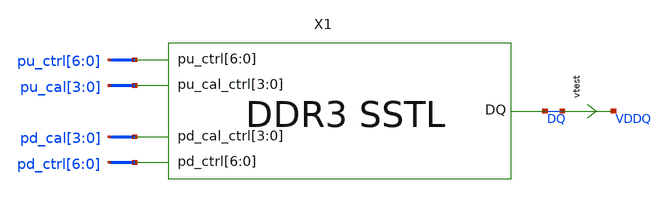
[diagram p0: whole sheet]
** sch_path: schem/sstl_res_tb.sch
* Copyright 2021 Stefan Frederik Schippers
* Licensed under the Apache License, Version 2.0 (the "License");
* you may not use this file except in compliance with the License.
* You may obtain a copy of the License at
* https://www.apache.org/licenses/LICENSE-2.0
* Unless required by applicable law or agreed to in writing, software
* distributed under the License is distributed on an "AS IS" BASIS,
* WITHOUT WARRANTIES OR CONDITIONS OF ANY KIND, either express or implied.
* See the License for the specific language governing permissions and
* limitations under the License.
**.subckt sstl_res_tb
vtest DQ VDDQ 0
.save i(vtest)
X1 DQ pd_ctrl[6] pd_ctrl[5] pd_ctrl[4] pd_ctrl[3] pd_ctrl[2] pd_ctrl[1] pd_ctrl[0] pu_ctrl[6]
+ pu_ctrl[5] pu_ctrl[4] pu_ctrl[3] pu_ctrl[2] pu_ctrl[1] pu_ctrl[0] pd_cal[3] pd_cal[2] pd_cal[1] pd_cal[0]
+ pu_cal[3] pu_cal[2] pu_cal[1] pu_cal[0] SSTL
**** begin user architecture code
 ** Local library links to pdk
.lib ./sky130/libs/SED_process_SED_lib.spice SED_process_SED
.include $::SKYWATER_STDCELLS/sky130_fd_sc_hd.spice

**** end user architecture code
**.ends

* expanding   symbol:  schem/SSTL.sym # of pins=5
** sym_path: schem/SSTL.sym
** sch_path: schem/SSTL.sch
.subckt SSTL DQ pd_ctrl[6] pd_ctrl[5] pd_ctrl[4] pd_ctrl[3] pd_ctrl[2] pd_ctrl[1] pd_ctrl[0]
+ pu_ctrl[6] pu_ctrl[5] pu_ctrl[4] pu_ctrl[3] pu_ctrl[2] pu_ctrl[1] pu_ctrl[0] pd_cal_ctrl[3] pd_cal_ctrl[2]
+ pd_cal_ctrl[1] pd_cal_ctrl[0] pu_cal_ctrl[3] pu_cal_ctrl[2] pu_cal_ctrl[1] pu_cal_ctrl[0]
*.iopin DQ
*.ipin pu_cal_ctrl[3],pu_cal_ctrl[2],pu_cal_ctrl[1],pu_cal_ctrl[0]
*.ipin pd_cal_ctrl[3],pd_cal_ctrl[2],pd_cal_ctrl[1],pd_cal_ctrl[0]
*.ipin pu_ctrl[6],pu_ctrl[5],pu_ctrl[4],pu_ctrl[3],pu_ctrl[2],pu_ctrl[1],pu_ctrl[0]
*.ipin pd_ctrl[6],pd_ctrl[5],pd_ctrl[4],pd_ctrl[3],pd_ctrl[2],pd_ctrl[1],pd_ctrl[0]
X1 DQ n_pu_ctrl[6] n_pu_cal_ctrl[3] n_pu_cal_ctrl[2] n_pu_cal_ctrl[1] n_pu_cal_ctrl[0] p-leg
X2 DQ pd_ctrl_buff[6] pd_cal_ctrl[3] pd_cal_ctrl[2] pd_cal_ctrl[1] pd_cal_ctrl[0] n-leg
X3 DQ n_pu_ctrl[5] n_pu_cal_ctrl[3] n_pu_cal_ctrl[2] n_pu_cal_ctrl[1] n_pu_cal_ctrl[0] p-leg
X4 DQ pd_ctrl_buff[5] pd_cal_ctrl[3] pd_cal_ctrl[2] pd_cal_ctrl[1] pd_cal_ctrl[0] n-leg
X5 DQ n_pu_ctrl[4] n_pu_cal_ctrl[3] n_pu_cal_ctrl[2] n_pu_cal_ctrl[1] n_pu_cal_ctrl[0] p-leg
X6 DQ pd_ctrl_buff[4] pd_cal_ctrl[3] pd_cal_ctrl[2] pd_cal_ctrl[1] pd_cal_ctrl[0] n-leg
X7 DQ n_pu_ctrl[3] n_pu_cal_ctrl[3] n_pu_cal_ctrl[2] n_pu_cal_ctrl[1] n_pu_cal_ctrl[0] p-leg
X8 DQ pd_ctrl_buff[3] pd_cal_ctrl[3] pd_cal_ctrl[2] pd_cal_ctrl[1] pd_cal_ctrl[0] n-leg
X9 DQ n_pu_ctrl[2] n_pu_cal_ctrl[3] n_pu_cal_ctrl[2] n_pu_cal_ctrl[1] n_pu_cal_ctrl[0] p-leg
X10 DQ pd_ctrl_buff[2] pd_cal_ctrl[3] pd_cal_ctrl[2] pd_cal_ctrl[1] pd_cal_ctrl[0] n-leg
X11 DQ n_pu_ctrl[1] n_pu_cal_ctrl[3] n_pu_cal_ctrl[2] n_pu_cal_ctrl[1] n_pu_cal_ctrl[0] p-leg
X12 DQ pd_ctrl_buff[1] pd_cal_ctrl[3] pd_cal_ctrl[2] pd_cal_ctrl[1] pd_cal_ctrl[0] n-leg
X13 DQ n_pu_ctrl[0] n_pu_cal_ctrl[3] n_pu_cal_ctrl[2] n_pu_cal_ctrl[1] n_pu_cal_ctrl[0] p-leg
X14 DQ pd_ctrl_buff[0] pd_cal_ctrl[3] pd_cal_ctrl[2] pd_cal_ctrl[1] pd_cal_ctrl[0] n-leg
xpd_buff_4[6] pdc2[6] VGND VNB VPB VPWR pdc4[6] sky130_fd_sc_hd__clkinv_4
xpd_buff_4[5] pdc2[5] VGND VNB VPB VPWR pdc4[5] sky130_fd_sc_hd__clkinv_4
xpd_buff_4[4] pdc2[4] VGND VNB VPB VPWR pdc4[4] sky130_fd_sc_hd__clkinv_4
xpd_buff_4[3] pdc2[3] VGND VNB VPB VPWR pdc4[3] sky130_fd_sc_hd__clkinv_4
xpd_buff_4[2] pdc2[2] VGND VNB VPB VPWR pdc4[2] sky130_fd_sc_hd__clkinv_4
xpd_buff_4[1] pdc2[1] VGND VNB VPB VPWR pdc4[1] sky130_fd_sc_hd__clkinv_4
xpd_buff_4[0] pdc2[0] VGND VNB VPB VPWR pdc4[0] sky130_fd_sc_hd__clkinv_4
xpd_buff_6[6] pdc4[6] VGND VNB VPB VPWR pd_ctrl_buff[6] sky130_fd_sc_hd__clkbuf_8
xpd_buff_6[5] pdc4[5] VGND VNB VPB VPWR pd_ctrl_buff[5] sky130_fd_sc_hd__clkbuf_8
xpd_buff_6[4] pdc4[4] VGND VNB VPB VPWR pd_ctrl_buff[4] sky130_fd_sc_hd__clkbuf_8
xpd_buff_6[3] pdc4[3] VGND VNB VPB VPWR pd_ctrl_buff[3] sky130_fd_sc_hd__clkbuf_8
xpd_buff_6[2] pdc4[2] VGND VNB VPB VPWR pd_ctrl_buff[2] sky130_fd_sc_hd__clkbuf_8
xpd_buff_6[1] pdc4[1] VGND VNB VPB VPWR pd_ctrl_buff[1] sky130_fd_sc_hd__clkbuf_8
xpd_buff_6[0] pdc4[0] VGND VNB VPB VPWR pd_ctrl_buff[0] sky130_fd_sc_hd__clkbuf_8
xpu_buff_4[6] pu_ctrl[6] VGND VNB VPB VPWR puc4[6] sky130_fd_sc_hd__clkbuf_16
xpu_buff_4[5] pu_ctrl[5] VGND VNB VPB VPWR puc4[5] sky130_fd_sc_hd__clkbuf_16
xpu_buff_4[4] pu_ctrl[4] VGND VNB VPB VPWR puc4[4] sky130_fd_sc_hd__clkbuf_16
xpu_buff_4[3] pu_ctrl[3] VGND VNB VPB VPWR puc4[3] sky130_fd_sc_hd__clkbuf_16
xpu_buff_4[2] pu_ctrl[2] VGND VNB VPB VPWR puc4[2] sky130_fd_sc_hd__clkbuf_16
xpu_buff_4[1] pu_ctrl[1] VGND VNB VPB VPWR puc4[1] sky130_fd_sc_hd__clkbuf_16
xpu_buff_4[0] pu_ctrl[0] VGND VNB VPB VPWR puc4[0] sky130_fd_sc_hd__clkbuf_16
xpu_buff_6[6] puc4[6] VGND VNB VPB VPWR n_pu_ctrl[6] sky130_fd_sc_hd__clkinv_16
xpu_buff_6[5] puc4[5] VGND VNB VPB VPWR n_pu_ctrl[5] sky130_fd_sc_hd__clkinv_16
xpu_buff_6[4] puc4[4] VGND VNB VPB VPWR n_pu_ctrl[4] sky130_fd_sc_hd__clkinv_16
xpu_buff_6[3] puc4[3] VGND VNB VPB VPWR n_pu_ctrl[3] sky130_fd_sc_hd__clkinv_16
xpu_buff_6[2] puc4[2] VGND VNB VPB VPWR n_pu_ctrl[2] sky130_fd_sc_hd__clkinv_16
xpu_buff_6[1] puc4[1] VGND VNB VPB VPWR n_pu_ctrl[1] sky130_fd_sc_hd__clkinv_16
xpu_buff_6[0] puc4[0] VGND VNB VPB VPWR n_pu_ctrl[0] sky130_fd_sc_hd__clkinv_16
xpu_cal_inv[3] pu_cal_ctrl[3] VGND VNB VPB VPWR n_pu_cal_ctrl[3] sky130_fd_sc_hd__inv_1
xpu_cal_inv[2] pu_cal_ctrl[2] VGND VNB VPB VPWR n_pu_cal_ctrl[2] sky130_fd_sc_hd__inv_1
xpu_cal_inv[1] pu_cal_ctrl[1] VGND VNB VPB VPWR n_pu_cal_ctrl[1] sky130_fd_sc_hd__inv_1
xpu_cal_inv[0] pu_cal_ctrl[0] VGND VNB VPB VPWR n_pu_cal_ctrl[0] sky130_fd_sc_hd__inv_1
V1 VDD VPWR 0
V2 VGND GND 0
V3 VDD VPB 0
V4 VNB GND 0
Vpd_ctrl_0 v_pd_ctrl_0 pd_ctrl_buff[6] 0
Vpd_ctrl_1 v_pu_ctrl_0 n_pu_ctrl[6] 0
xpu_buff_2[6] puc4[6] VGND VNB VPB VPWR n_pu_ctrl[6] sky130_fd_sc_hd__clkinv_16
xpu_buff_2[5] puc4[5] VGND VNB VPB VPWR n_pu_ctrl[5] sky130_fd_sc_hd__clkinv_16
xpu_buff_2[4] puc4[4] VGND VNB VPB VPWR n_pu_ctrl[4] sky130_fd_sc_hd__clkinv_16
xpu_buff_2[3] puc4[3] VGND VNB VPB VPWR n_pu_ctrl[3] sky130_fd_sc_hd__clkinv_16
xpu_buff_2[2] puc4[2] VGND VNB VPB VPWR n_pu_ctrl[2] sky130_fd_sc_hd__clkinv_16
xpu_buff_2[1] puc4[1] VGND VNB VPB VPWR n_pu_ctrl[1] sky130_fd_sc_hd__clkinv_16
xpu_buff_2[0] puc4[0] VGND VNB VPB VPWR n_pu_ctrl[0] sky130_fd_sc_hd__clkinv_16
xpd_buff_1[6] pd_ctrl[6] VGND VNB VPB VPWR pdc2[6] sky130_fd_sc_hd__clkinv_4
xpd_buff_1[5] pd_ctrl[5] VGND VNB VPB VPWR pdc2[5] sky130_fd_sc_hd__clkinv_4
xpd_buff_1[4] pd_ctrl[4] VGND VNB VPB VPWR pdc2[4] sky130_fd_sc_hd__clkinv_4
xpd_buff_1[3] pd_ctrl[3] VGND VNB VPB VPWR pdc2[3] sky130_fd_sc_hd__clkinv_4
xpd_buff_1[2] pd_ctrl[2] VGND VNB VPB VPWR pdc2[2] sky130_fd_sc_hd__clkinv_4
xpd_buff_1[1] pd_ctrl[1] VGND VNB VPB VPWR pdc2[1] sky130_fd_sc_hd__clkinv_4
xpd_buff_1[0] pd_ctrl[0] VGND VNB VPB VPWR pdc2[0] sky130_fd_sc_hd__clkinv_4
xpu_buff_1[6] puc4[6] VGND VNB VPB VPWR n_pu_ctrl[6] sky130_fd_sc_hd__clkinv_16
xpu_buff_1[5] puc4[5] VGND VNB VPB VPWR n_pu_ctrl[5] sky130_fd_sc_hd__clkinv_16
xpu_buff_1[4] puc4[4] VGND VNB VPB VPWR n_pu_ctrl[4] sky130_fd_sc_hd__clkinv_16
xpu_buff_1[3] puc4[3] VGND VNB VPB VPWR n_pu_ctrl[3] sky130_fd_sc_hd__clkinv_16
xpu_buff_1[2] puc4[2] VGND VNB VPB VPWR n_pu_ctrl[2] sky130_fd_sc_hd__clkinv_16
xpu_buff_1[1] puc4[1] VGND VNB VPB VPWR n_pu_ctrl[1] sky130_fd_sc_hd__clkinv_16
xpu_buff_1[0] puc4[0] VGND VNB VPB VPWR n_pu_ctrl[0] sky130_fd_sc_hd__clkinv_16
.ends


* expanding   symbol:  p-leg.sym # of pins=3
** sym_path: schem/p-leg.sym
** sch_path: schem/p-leg.sch
.subckt p-leg DQ n_pu_ctrl n_cal_ctrl[3] n_cal_ctrl[2] n_cal_ctrl[1] n_cal_ctrl[0]
*.ipin n_cal_ctrl[3],n_cal_ctrl[2],n_cal_ctrl[1],n_cal_ctrl[0]
*.ipin n_pu_ctrl
*.iopin DQ
XR1 DQ net1 sky130_fd_pr__res_generic_po W=0.33 L=1.8 m=1
XMpullup net1 n_pu_ctrl VDD VDD sky130_fd_pr__pfet_01v8_lvt L=0.35 W=1 nf=1 ad='int((nf+1)/2) * W/nf * 0.29'
+ as='int((nf+2)/2) * W/nf * 0.29' pd='2*int((nf+1)/2) * (W/nf + 0.29)' ps='2*int((nf+2)/2) * (W/nf + 0.29)'
+ nrd='0.29 / W' nrs='0.29 / W' sa=0 sb=0 sd=0 mult=128 m=128
XMctrltot VDD n_cal_ctrl[0] VDD VDD sky130_fd_pr__pfet_01v8_lvt L=0.35 W=1 nf=1 ad='int((nf+1)/2) * W/nf * 0.29'
+ as='int((nf+2)/2) * W/nf * 0.29' pd='2*int((nf+1)/2) * (W/nf + 0.29)' ps='2*int((nf+2)/2) * (W/nf + 0.29)'
+ nrd='0.29 / W' nrs='0.29 / W' sa=0 sb=0 sd=0 mult=120 m=120
XMctrl0 DQ n_cal_ctrl[0] net1 VDD sky130_fd_pr__pfet_01v8_lvt L=0.35 W=1 nf=1 ad='int((nf+1)/2) * W/nf * 0.29'
+ as='int((nf+2)/2) * W/nf * 0.29' pd='2*int((nf+1)/2) * (W/nf + 0.29)' ps='2*int((nf+2)/2) * (W/nf + 0.29)'
+ nrd='0.29 / W' nrs='0.29 / W' sa=0 sb=0 sd=0 mult=48 m=48
XMctrl1 DQ n_cal_ctrl[1] net1 VDD sky130_fd_pr__pfet_01v8_lvt L=0.35 W=1 nf=1 ad='int((nf+1)/2) * W/nf * 0.29'
+ as='int((nf+2)/2) * W/nf * 0.29' pd='2*int((nf+1)/2) * (W/nf + 0.29)' ps='2*int((nf+2)/2) * (W/nf + 0.29)'
+ nrd='0.29 / W' nrs='0.29 / W' sa=0 sb=0 sd=0 mult=16 m=16
XMctrl2 DQ n_cal_ctrl[2] net1 VDD sky130_fd_pr__pfet_01v8_lvt L=0.35 W=1 nf=1 ad='int((nf+1)/2) * W/nf * 0.29'
+ as='int((nf+2)/2) * W/nf * 0.29' pd='2*int((nf+1)/2) * (W/nf + 0.29)' ps='2*int((nf+2)/2) * (W/nf + 0.29)'
+ nrd='0.29 / W' nrs='0.29 / W' sa=0 sb=0 sd=0 mult=8 m=8
XMctrl3 DQ n_cal_ctrl[3] net1 VDD sky130_fd_pr__pfet_01v8_lvt L=0.35 W=1 nf=1 ad='int((nf+1)/2) * W/nf * 0.29'
+ as='int((nf+2)/2) * W/nf * 0.29' pd='2*int((nf+1)/2) * (W/nf + 0.29)' ps='2*int((nf+2)/2) * (W/nf + 0.29)'
+ nrd='0.29 / W' nrs='0.29 / W' sa=0 sb=0 sd=0 mult=4 m=4
.ends


* expanding   symbol:  n-leg.sym # of pins=3
** sym_path: schem/n-leg.sym
** sch_path: schem/n-leg.sch
.subckt n-leg DQ pd_ctrl cal_ctrl[3] cal_ctrl[2] cal_ctrl[1] cal_ctrl[0]
*.iopin DQ
*.ipin pd_ctrl
*.ipin cal_ctrl[3],cal_ctrl[2],cal_ctrl[1],cal_ctrl[0]
XR1 vpulldown DQ sky130_fd_pr__res_generic_po W=0.33 L=1.7 m=1
Xn1 vpulldown pd_ctrl GND GND sky130_fd_pr__nfet_01v8 L=0.15 W=0.65 nf=1 ad='int((nf+1)/2) * W/nf * 0.29'
+ as='int((nf+2)/2) * W/nf * 0.29' pd='2*int((nf+1)/2) * (W/nf + 0.29)' ps='2*int((nf+2)/2) * (W/nf + 0.29)'
+ nrd='0.29 / W' nrs='0.29 / W' sa=0 sb=0 sd=0 mult=48 m=48
Xnctrl0 DQ cal_ctrl[0] vpulldown GND sky130_fd_pr__nfet_01v8 L=0.15 W=0.65 nf=1 ad='int((nf+1)/2) * W/nf * 0.29'
+ as='int((nf+2)/2) * W/nf * 0.29' pd='2*int((nf+1)/2) * (W/nf + 0.29)' ps='2*int((nf+2)/2) * (W/nf + 0.29)'
+ nrd='0.29 / W' nrs='0.29 / W' sa=0 sb=0 sd=0 mult=6 m=6
Xnctrl1 DQ cal_ctrl[1] vpulldown GND sky130_fd_pr__nfet_01v8 L=0.15 W=0.65 nf=1 ad='int((nf+1)/2) * W/nf * 0.29'
+ as='int((nf+2)/2) * W/nf * 0.29' pd='2*int((nf+1)/2) * (W/nf + 0.29)' ps='2*int((nf+2)/2) * (W/nf + 0.29)'
+ nrd='0.29 / W' nrs='0.29 / W' sa=0 sb=0 sd=0 mult=3 m=3
Xnctrl2 DQ cal_ctrl[2] vpulldown GND sky130_fd_pr__nfet_01v8 L=0.15 W=0.975 nf=1 ad='int((nf+1)/2) * W/nf * 0.29'
+ as='int((nf+2)/2) * W/nf * 0.29' pd='2*int((nf+1)/2) * (W/nf + 0.29)' ps='2*int((nf+2)/2) * (W/nf + 0.29)'
+ nrd='0.29 / W' nrs='0.29 / W' sa=0 sb=0 sd=0 mult=1 m=1
Xnctrl3 DQ cal_ctrl[3] vpulldown GND sky130_fd_pr__nfet_01v8 L=0.15 W=0.5 nf=1 ad='int((nf+1)/2) * W/nf * 0.29'
+ as='int((nf+2)/2) * W/nf * 0.29' pd='2*int((nf+1)/2) * (W/nf + 0.29)' ps='2*int((nf+2)/2) * (W/nf + 0.29)'
+ nrd='0.29 / W' nrs='0.29 / W' sa=0 sb=0 sd=0 mult=1 m=1
Xnctrl_tot GND GND GND GND sky130_fd_pr__nfet_01v8 L=0.15 W=0.65 nf=1 ad='int((nf+1)/2) * W/nf * 0.29'
+ as='int((nf+2)/2) * W/nf * 0.29' pd='2*int((nf+1)/2) * (W/nf + 0.29)' ps='2*int((nf+2)/2) * (W/nf + 0.29)'
+ nrd='0.29 / W' nrs='0.29 / W' sa=0 sb=0 sd=0 mult=11 m=11
.ends

.GLOBAL VDD
.GLOBAL GND
**** begin user architecture code


* power voltage
vvddq VDDQ 0 0
vvdd VDD 0 SED_vdd_SED

** CALIBRATION CONTROL **
* PULLUP
vpu_cal0 pu_cal[0] 0 SED_pucal0_SED
vpu_cal1 pu_cal[1] 0 SED_pucal1_SED
vpu_cal2 pu_cal[2] 0 SED_pucal2_SED
vpu_cal3 pu_cal[3] 0 SED_pucal3_SED
* PULLDOWN
vpd_cal0 pd_cal[0] 0 SED_pdcal0_SED
vpd_cal1 pd_cal[1] 0 SED_pdcal1_SED
vpd_cal2 pd_cal[2] 0 SED_pdcal2_SED
vpd_cal3 pd_cal[3] 0 SED_pdcal3_SED

** LEG ENABLE/DISABLE CONTROL
* PULLUP
vpu_ctrl0 pu_ctrl[0] 0 SED_puctrl0_SED
vpu_ctrl1 pu_ctrl[1] 0 SED_puctrl1_SED
vpu_ctrl2 pu_ctrl[2] 0 SED_puctrl2_SED
vpu_ctrl3 pu_ctrl[3] 0 SED_puctrl3_SED
vpu_ctrl4 pu_ctrl[4] 0 SED_puctrl4_SED
vpu_ctrl5 pu_ctrl[5] 0 SED_puctrl5_SED
vpu_ctrl6 pu_ctrl[6] 0 SED_puctrl6_SED
* PULLDOWN
vpd_ctrl0 pd_ctrl[0] 0 SED_pdctrl0_SED
vpd_ctrl1 pd_ctrl[1] 0 SED_pdctrl1_SED
vpd_ctrl2 pd_ctrl[2] 0 SED_pdctrl2_SED
vpd_ctrl3 pd_ctrl[3] 0 SED_pdctrl3_SED
vpd_ctrl4 pd_ctrl[4] 0 SED_pdctrl4_SED
vpd_ctrl5 pd_ctrl[5] 0 SED_pdctrl5_SED
vpd_ctrl6 pd_ctrl[6] 0 SED_pdctrl6_SED


.control
set num_threads=1
save all
set temp=SED_temp_SED

* RUN SIMULATION
dc vvddq 0.3 1.2 0.05
* OUTPUT
print i(vtest)
wrdata out/SED_plotName_SED/SED_plotName_SED.txt i(vtest)
set hcopydevtype = svg
hardcopy ./out/SED_plotName_SED/SED_plotName_SED.svg I(vtest) vs vddq title 'Resistance vs pin voltage'

.endc


**** end user architecture code
.end
